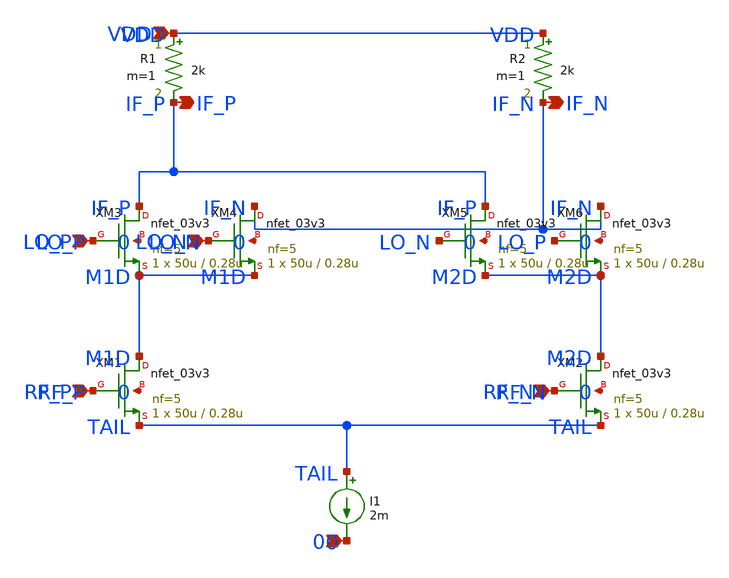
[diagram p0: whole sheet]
** sch_path: modules/PandaChip/designs/rf_trans/mixer.sch
**.subckt mixer VDD 0 RF_P RF_N LO_P LO_N IF_P IF_N
*.ipin VDD
*.ipin 0
*.ipin RF_P
*.ipin RF_N
*.ipin LO_P
*.ipin LO_N
*.opin IF_P
*.opin IF_N
XM1 M1D RF_P TAIL 0 nfet_03v3 L=0.28u W=50u nf=5 ad='int((nf+1)/2) * W/nf * 0.18u' as='int((nf+2)/2) * W/nf * 0.18u'
+ pd='2*int((nf+1)/2) * (W/nf + 0.18u)' ps='2*int((nf+2)/2) * (W/nf + 0.18u)' nrd='0.18u / W' nrs='0.18u / W'
+ sa=0 sb=0 sd=0 m=1
XM2 M2D RF_N TAIL 0 nfet_03v3 L=0.28u W=50u nf=5 ad='int((nf+1)/2) * W/nf * 0.18u' as='int((nf+2)/2) * W/nf * 0.18u'
+ pd='2*int((nf+1)/2) * (W/nf + 0.18u)' ps='2*int((nf+2)/2) * (W/nf + 0.18u)' nrd='0.18u / W' nrs='0.18u / W'
+ sa=0 sb=0 sd=0 m=1
XM3 IF_P LO_P M1D 0 nfet_03v3 L=0.28u W=50u nf=5 ad='int((nf+1)/2) * W/nf * 0.18u' as='int((nf+2)/2) * W/nf * 0.18u'
+ pd='2*int((nf+1)/2) * (W/nf + 0.18u)' ps='2*int((nf+2)/2) * (W/nf + 0.18u)' nrd='0.18u / W' nrs='0.18u / W'
+ sa=0 sb=0 sd=0 m=1
XM4 IF_N LO_N M1D 0 nfet_03v3 L=0.28u W=50u nf=5 ad='int((nf+1)/2) * W/nf * 0.18u' as='int((nf+2)/2) * W/nf * 0.18u'
+ pd='2*int((nf+1)/2) * (W/nf + 0.18u)' ps='2*int((nf+2)/2) * (W/nf + 0.18u)' nrd='0.18u / W' nrs='0.18u / W'
+ sa=0 sb=0 sd=0 m=1
XM5 IF_P LO_N M2D 0 nfet_03v3 L=0.28u W=50u nf=5 ad='int((nf+1)/2) * W/nf * 0.18u' as='int((nf+2)/2) * W/nf * 0.18u'
+ pd='2*int((nf+1)/2) * (W/nf + 0.18u)' ps='2*int((nf+2)/2) * (W/nf + 0.18u)' nrd='0.18u / W' nrs='0.18u / W'
+ sa=0 sb=0 sd=0 m=1
XM6 IF_N LO_P M2D 0 nfet_03v3 L=0.28u W=50u nf=5 ad='int((nf+1)/2) * W/nf * 0.18u' as='int((nf+2)/2) * W/nf * 0.18u'
+ pd='2*int((nf+1)/2) * (W/nf + 0.18u)' ps='2*int((nf+2)/2) * (W/nf + 0.18u)' nrd='0.18u / W' nrs='0.18u / W'
+ sa=0 sb=0 sd=0 m=1
R1 VDD IF_P 2k m=1
R2 VDD IF_N 2k m=1
I1 TAIL 0 2m
**.ends
.end
